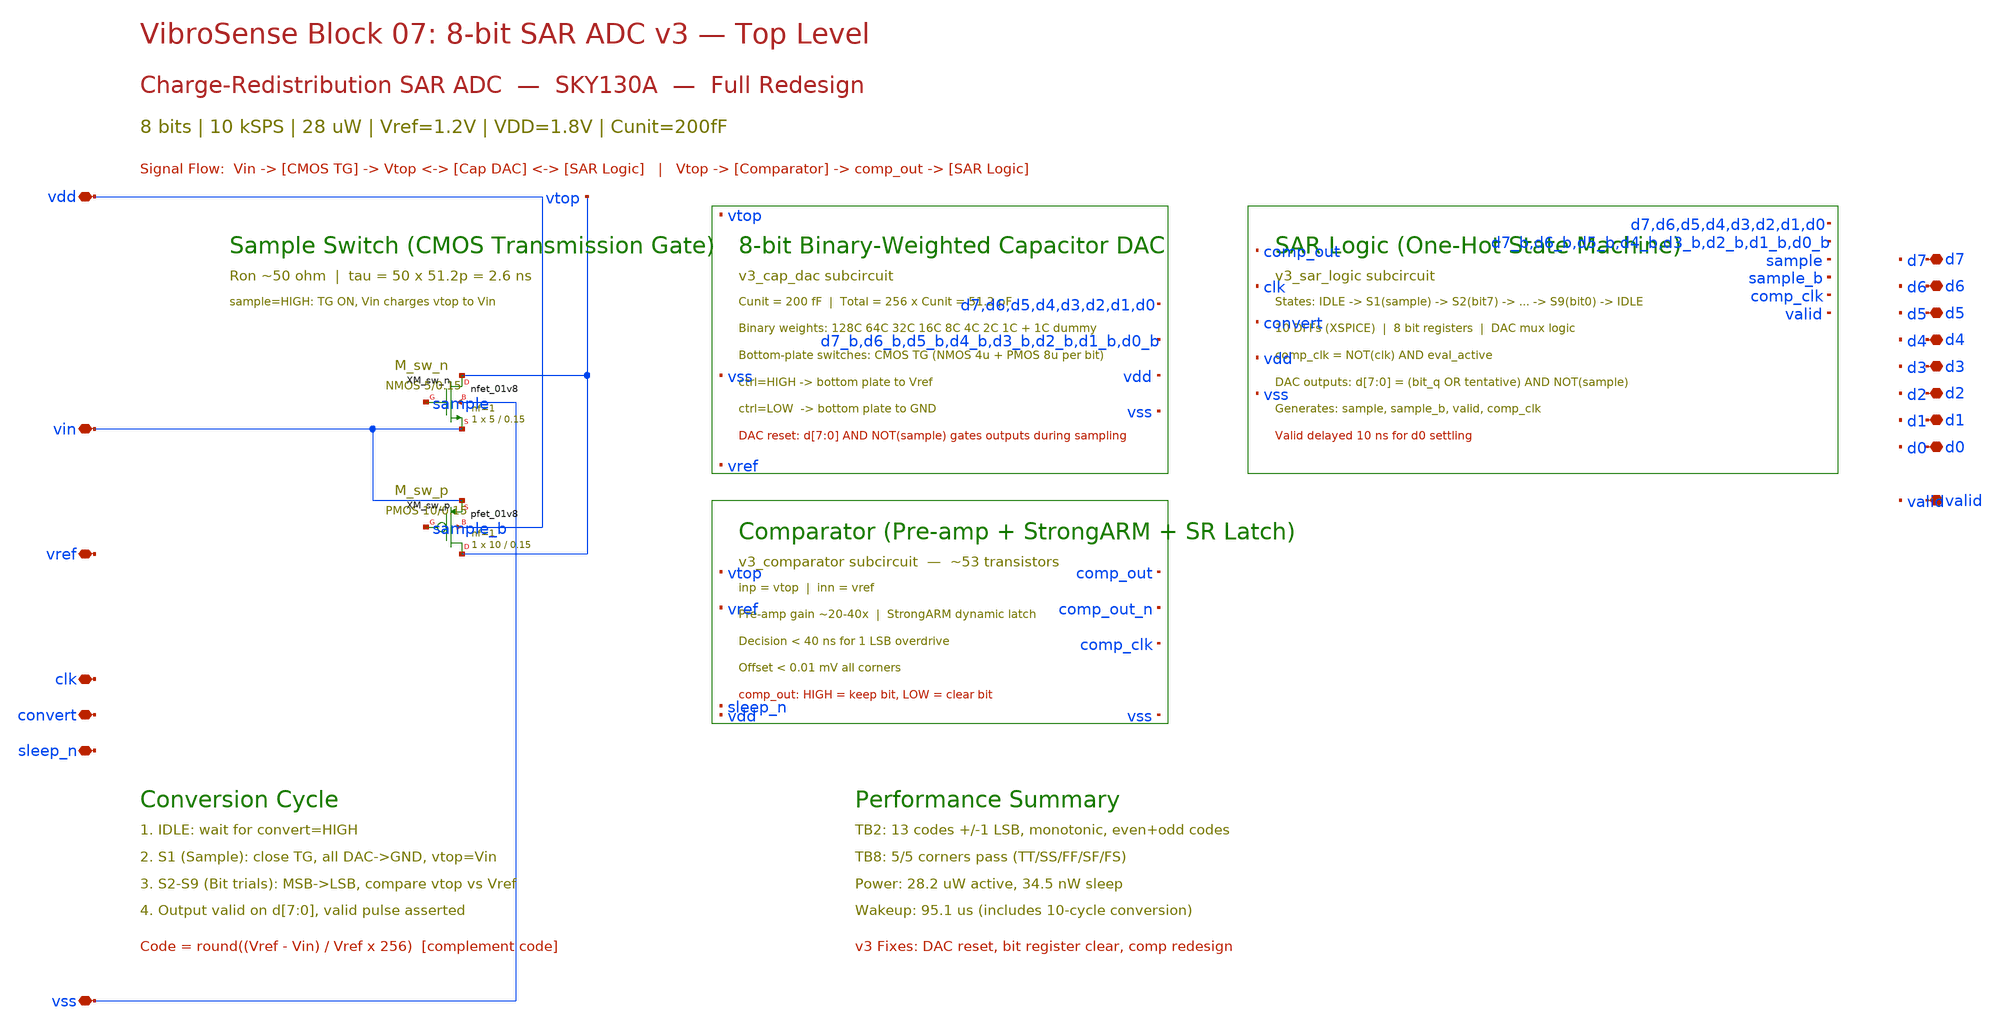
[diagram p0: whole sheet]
** sch_path: vibrosense/07_adc_v3/v3_sar_adc.sch
**.subckt v3_sar_adc vin vdd vss vref clk convert sleep_n d7 d6 d5 d4 d3 d2 d1 d0 valid
*.iopin vin
*.iopin vdd
*.iopin vss
*.iopin vref
*.iopin clk
*.iopin convert
*.iopin sleep_n
*.iopin d7
*.iopin d6
*.iopin d5
*.iopin d4
*.iopin d3
*.iopin d2
*.iopin d1
*.iopin d0
*.iopin valid
XXM_sw_n vtop sample vin vss sky130_fd_pr__nfet_01v8 L=0.15 W=5 nf=1 ad='int((1 + 1)/2) * 5 / 1 * 0.29'
+ as='int((1 + 2)/2) * 5 / 1 * 0.29' pd='2*int((1 + 1)/2) * (5 / 1 + 0.29)' ps='2*int((1 + 2)/2) * (5 / 1 + 0.29)'
+ nrd='0.29 / 5 ' nrs='0.29 / 5 ' sa=0 sb=0 sd=0 mult=1 m=1
XXM_sw_p vtop sample_b vin vdd sky130_fd_pr__pfet_01v8 L=0.15 W=10 nf=1 ad='int((nf+1)/2) * W/nf * 0.29'
+ as='int((nf+2)/2) * W/nf * 0.29' pd='2*int((nf+1)/2) * (W/nf + 0.29)' ps='2*int((nf+2)/2) * (W/nf + 0.29)'
+ nrd='0.29 / W' nrs='0.29 / W' sa=0 sb=0 sd=0 mult=1 m=1
**.ends
.end
